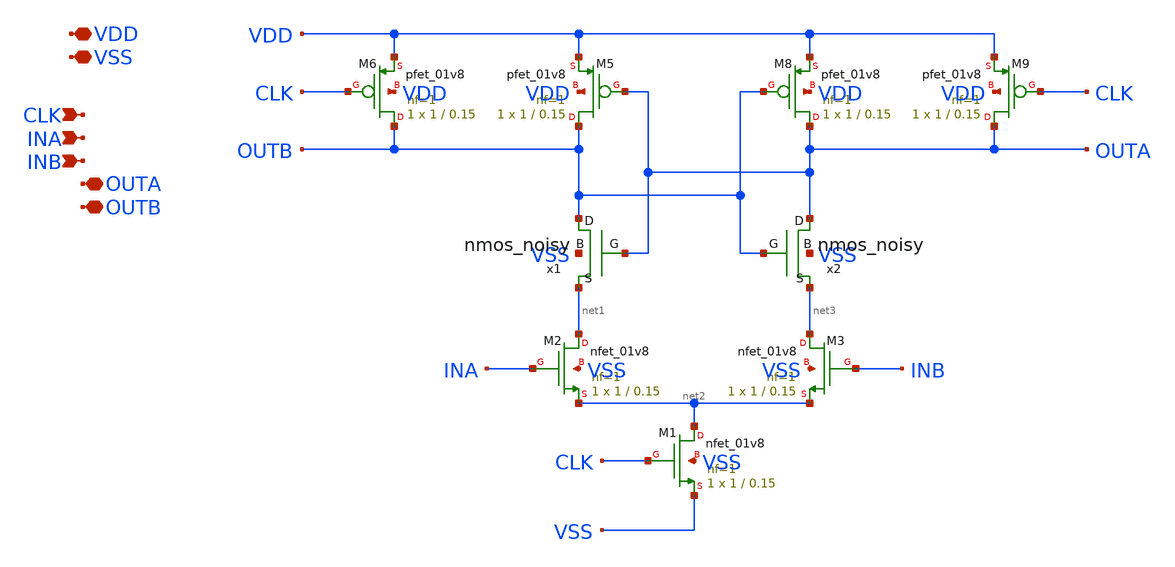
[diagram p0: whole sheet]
** sch_path: comp1_noisy.sch
**.subckt comp1_noisy VSS VDD OUTB OUTA INB INA CLK
*.iopin VSS
*.iopin VDD
*.iopin OUTB
*.iopin OUTA
*.ipin INB
*.ipin INA
*.ipin CLK
XM1 net2 CLK VSS VSS sky130_fd_pr__nfet_01v8 L=0.15 W=1 nf=1 ad='int((nf+1)/2) * W/nf * 0.29' as='int((nf+2)/2) * W/nf * 0.29'
+ pd='2*int((nf+1)/2) * (W/nf + 0.29)' ps='2*int((nf+2)/2) * (W/nf + 0.29)' nrd='0.29 / W' nrs='0.29 / W'
+ sa=0 sb=0 sd=0 mult=1 m=1
XM2 net1 INA net2 VSS sky130_fd_pr__nfet_01v8 L=0.15 W=1 nf=1 ad='int((nf+1)/2) * W/nf * 0.29' as='int((nf+2)/2) * W/nf * 0.29'
+ pd='2*int((nf+1)/2) * (W/nf + 0.29)' ps='2*int((nf+2)/2) * (W/nf + 0.29)' nrd='0.29 / W' nrs='0.29 / W'
+ sa=0 sb=0 sd=0 mult=1 m=1
XM5 OUTB OUTA VDD VDD sky130_fd_pr__pfet_01v8 L=0.15 W=1 nf=1 ad='int((nf+1)/2) * W/nf * 0.29' as='int((nf+2)/2) * W/nf * 0.29'
+ pd='2*int((nf+1)/2) * (W/nf + 0.29)' ps='2*int((nf+2)/2) * (W/nf + 0.29)' nrd='0.29 / W' nrs='0.29 / W'
+ sa=0 sb=0 sd=0 mult=1 m=1
XM6 OUTB CLK VDD VDD sky130_fd_pr__pfet_01v8 L=0.15 W=1 nf=1 ad='int((nf+1)/2) * W/nf * 0.29' as='int((nf+2)/2) * W/nf * 0.29'
+ pd='2*int((nf+1)/2) * (W/nf + 0.29)' ps='2*int((nf+2)/2) * (W/nf + 0.29)' nrd='0.29 / W' nrs='0.29 / W'
+ sa=0 sb=0 sd=0 mult=1 m=1
XM3 net3 INB net2 VSS sky130_fd_pr__nfet_01v8 L=0.15 W=1 nf=1 ad='int((nf+1)/2) * W/nf * 0.29' as='int((nf+2)/2) * W/nf * 0.29'
+ pd='2*int((nf+1)/2) * (W/nf + 0.29)' ps='2*int((nf+2)/2) * (W/nf + 0.29)' nrd='0.29 / W' nrs='0.29 / W'
+ sa=0 sb=0 sd=0 mult=1 m=1
XM8 OUTA OUTB VDD VDD sky130_fd_pr__pfet_01v8 L=0.15 W=1 nf=1 ad='int((nf+1)/2) * W/nf * 0.29' as='int((nf+2)/2) * W/nf * 0.29'
+ pd='2*int((nf+1)/2) * (W/nf + 0.29)' ps='2*int((nf+2)/2) * (W/nf + 0.29)' nrd='0.29 / W' nrs='0.29 / W'
+ sa=0 sb=0 sd=0 mult=1 m=1
XM9 OUTA CLK VDD VDD sky130_fd_pr__pfet_01v8 L=0.15 W=1 nf=1 ad='int((nf+1)/2) * W/nf * 0.29' as='int((nf+2)/2) * W/nf * 0.29'
+ pd='2*int((nf+1)/2) * (W/nf + 0.29)' ps='2*int((nf+2)/2) * (W/nf + 0.29)' nrd='0.29 / W' nrs='0.29 / W'
+ sa=0 sb=0 sd=0 mult=1 m=1
x1 VSS OUTB OUTA net1 nmos_noisy
x2 VSS OUTA OUTB net3 nmos_noisy
**.ends

* expanding   symbol:  /home/users/dstanley/EE272B/xschem_tests/nmos_noisy.sym # of pins=4
** sym_path: nmos_noisy.sym
** sch_path: nmos_noisy.sch
.subckt nmos_noisy B D G S
*.iopin S
*.ipin G
*.iopin D
*.ipin B
XM1 net1 G S B sky130_fd_pr__nfet_01v8 L=0.15 W=1 nf=1 ad='int((nf+1)/2) * W/nf * 0.29' as='int((nf+2)/2) * W/nf * 0.29'
+ pd='2*int((nf+1)/2) * (W/nf + 0.29)' ps='2*int((nf+2)/2) * (W/nf + 0.29)' nrd='0.29 / W' nrs='0.29 / W'
+ sa=0 sb=0 sd=0 mult=1 m=1
V1 noise_node S DC 0 trnoise(0 {noise_timestep} {oneoverf_exponent} {oneoverf_rms})
**** begin user architecture code

.param noise_max_freq=100MEG
.param noise_timestep={1/noise_max_freq}
.param oneoverf_exponent=0.8
.param oneoverf_rms=6.63n
.param i_nominal=14.46u

**** end user architecture code
B1 D S I = i(V2)/{i_nominal}*v(noise_node, S)
V2 D net1 dc 0
R1 noise_node S 1k m=1
.ends

.end
